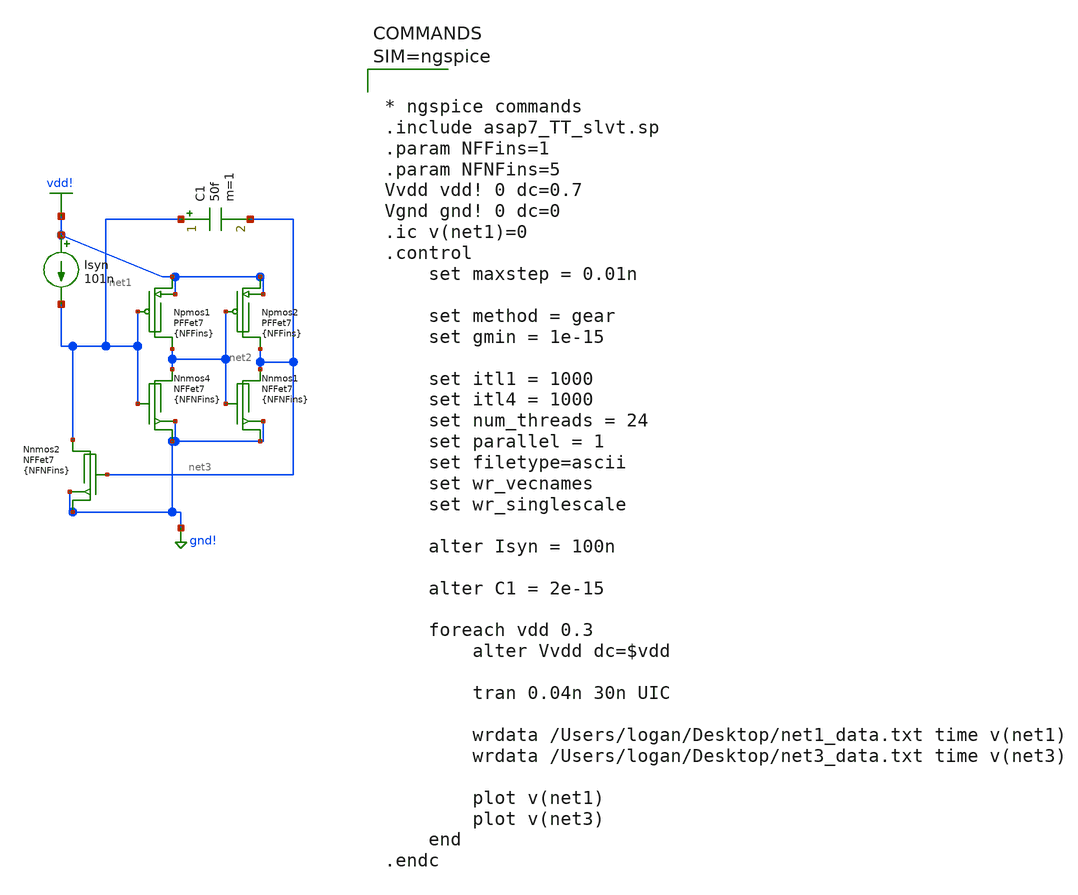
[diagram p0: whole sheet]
** sch_path: SimulationModeling/DannevillePlotting.sch
**.subckt DannevillePlotting
Isyn vdd! net1 101n
Npmos1 vdd! net1 net2 vdd! BSIMCMG_osdi_P nfin={NFFins}
Nnmos4 gnd! net1 net2 gnd! BSIMCMG_osdi_N nfin={NFNFins}
Npmos2 vdd! net2 net3 vdd! BSIMCMG_osdi_P nfin={NFFins}
Nnmos1 gnd! net2 net3 gnd! BSIMCMG_osdi_N nfin={NFNFins}
C1 net1 net3 50f m=1
Nnmos2 gnd! net3 net1 gnd! BSIMCMG_osdi_N nfin={NFNFins}
**** begin user architecture code



* ngspice commands
.include asap7_TT_slvt.sp
.param NFFins=1
.param NFNFins=5
Vvdd vdd! 0 dc=0.7
Vgnd gnd! 0 dc=0
.ic v(net1)=0
.control
    set maxstep = 0.01n

    set method = gear
    set gmin = 1e-15

    set itl1 = 1000
    set itl4 = 1000
    set num_threads = 24
    set parallel = 1
    set filetype=ascii
    set wr_vecnames
    set wr_singlescale

    alter Isyn = 100n

    alter C1 = 2e-15

    foreach vdd 0.3
        alter Vvdd dc=$vdd

        tran 0.04n 30n UIC

        wrdata /Users/logan/Desktop/net1_data.txt time v(net1)
        wrdata /Users/logan/Desktop/net3_data.txt time v(net3)

        plot v(net1)
        plot v(net3)
    end
.endc



**** end user architecture code
**.ends
.GLOBAL gnd!
.GLOBAL vdd!
.end
